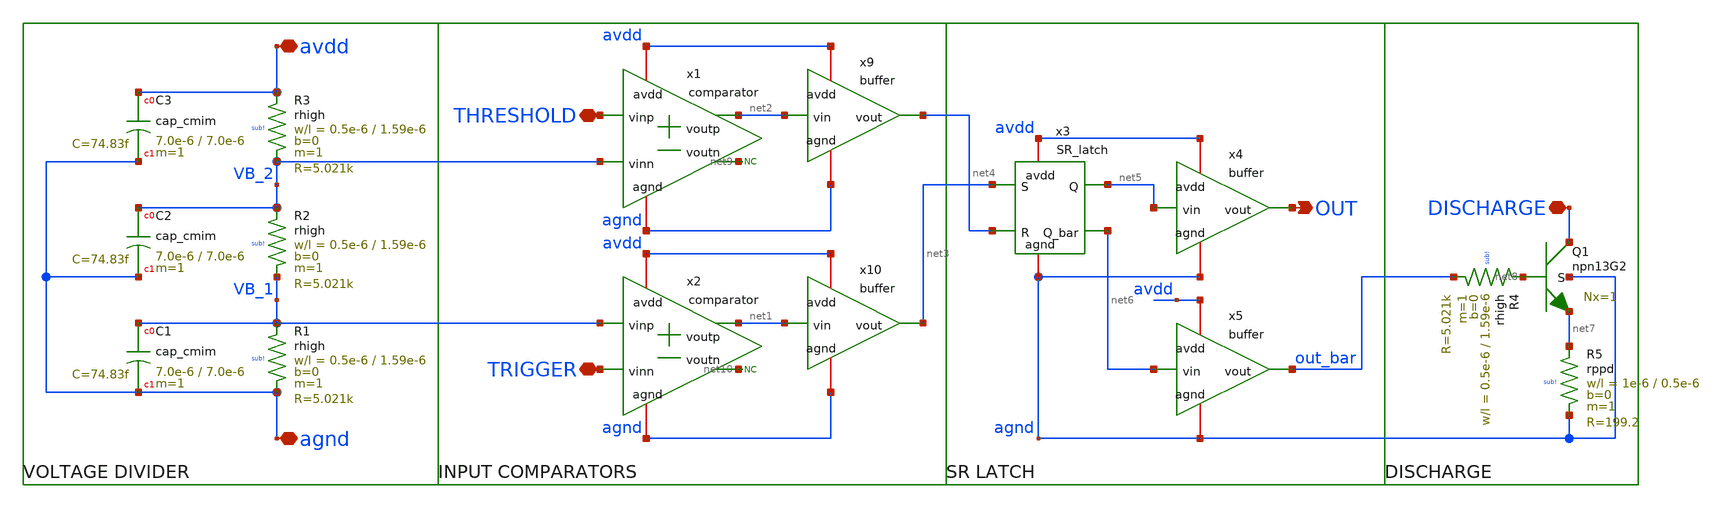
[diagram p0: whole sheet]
** sch_path: xschem/555.sch
**.subckt 555 OUT avdd agnd TRIGGER THRESHOLD DISCHARGE
*.opin OUT
*.iopin avdd
*.iopin agnd
*.iopin TRIGGER
*.iopin THRESHOLD
*.iopin DISCHARGE
XR3 avdd VB_2 sub! rhigh w=0.5e-6 l=1.59e-6 m=1 b=0 mm_ok=1
XR1 VB_1 agnd sub! rhigh w=0.5e-6 l=1.59e-6 m=1 b=0 mm_ok=1
XR2 VB_2 VB_1 sub! rhigh w=0.5e-6 l=1.59e-6 m=1 b=0 mm_ok=1
XC1 VB_1 agnd cap_cmim w=7.0e-6 l=7.0e-6 m=1 mm_ok=1
XC2 VB_2 agnd cap_cmim w=7.0e-6 l=7.0e-6 m=1 mm_ok=1
XC3 avdd agnd cap_cmim w=7.0e-6 l=7.0e-6 m=1 mm_ok=1
XR4 net8 out_bar sub! rhigh w=0.5e-6 l=1.59e-6 m=1 b=0 mm_ok=1
x1 avdd net2 net9 VB_2 THRESHOLD agnd comparator
x2 avdd net1 net10 TRIGGER VB_1 agnd comparator
x9 avdd net2 net4 agnd buffer
x10 avdd net1 net3 agnd buffer
x3 avdd net6 net5 agnd net3 net4 SR_latch
x4 avdd net5 OUT agnd buffer
x5 avdd net6 out_bar agnd buffer
* noconn #net9
* noconn #net10
XQ1 DISCHARGE net8 net7 agnd npn13G2 Nx=1 mm_ok=1
XR5 net7 agnd sub! rppd w=1e-6 l=0.5e-6 m=1 b=0 mm_ok=1
**.ends

* expanding   symbol:  comparator.sym # of pins=6
** sym_path: xschem/comparator.sym
** sch_path: xschem/comparator.sch
.subckt comparator avdd voutp voutn vinn vinp agnd
*.iopin avdd
*.ipin vinp
*.opin voutp
*.iopin agnd
*.ipin vinn
*.opin voutn
XQ1 voutp vinn net1 agnd npn13G2 Nx=1 mm_ok=1
XR1 avdd voutp sub! rppd w=0.5e-6 l=7.5e-6 m=1 b=0 mm_ok=1
XR2 net1 agnd sub! rppd w=0.5e-6 l=0.5e-6 m=1 b=0 mm_ok=1
XR3 avdd voutn sub! rppd w=0.5e-6 l=7.5e-6 m=1 b=0 mm_ok=1
XQ2 voutn vinp net1 agnd npn13G2 Nx=1 mm_ok=1
.ends


* expanding   symbol:  buffer.sym # of pins=4
** sym_path: xschem/buffer.sym
** sch_path: xschem/buffer.sch
.subckt buffer avdd vin vout agnd
*.iopin avdd
*.ipin vin
*.opin vout
*.iopin agnd
x1 avdd vin net1 agnd inverter
x2 avdd net1 vout agnd inverter
.ends


* expanding   symbol:  SR_latch.sym # of pins=6
** sym_path: xschem/SR_latch.sym
** sch_path: xschem/SR_latch.sch
.subckt SR_latch avdd Q_bar Q agnd S R
*.ipin R
*.opin Q_bar
*.ipin S
*.opin Q
*.iopin avdd
*.iopin agnd
XQ2 Q_bar net2 agnd agnd npn13G2 Nx=1 mm_ok=1
XQ1 Q net1 agnd agnd npn13G2 Nx=1 mm_ok=1
XR3 net1 R sub! rppd w=0.5e-6 l=20e-6 m=1 b=0 mm_ok=1
XR1 S net2 sub! rppd w=0.5e-6 l=20e-6 m=1 b=0 mm_ok=1
XR2 net1 agnd sub! rhigh w=0.5e-6 l=20e-6 m=1 b=0 mm_ok=1
XR4 net2 agnd sub! rhigh w=0.5e-6 l=20e-6 m=1 b=0 mm_ok=1
XR5 net2 Q sub! rppd w=0.5e-6 l=20e-6 m=1 b=0 mm_ok=1
XR6 Q_bar net1 sub! rppd w=0.5e-6 l=20e-6 m=1 b=0 mm_ok=1
XR7 avdd Q sub! rppd w=0.5e-6 l=2e-6 m=1 b=0 mm_ok=1
XR8 avdd Q_bar sub! rppd w=0.5e-6 l=2e-6 m=1 b=0 mm_ok=1
.ends


* expanding   symbol:  inverter.sym # of pins=4
** sym_path: xschem/inverter.sym
** sch_path: xschem/inverter.sch
.subckt inverter avdd vin vout agnd
*.iopin avdd
*.ipin vin
*.opin vout
*.iopin agnd
XQ1 vout base agnd agnd npn13G2 Nx=10 mm_ok=1
XR1 avdd vout sub! rhigh w=1e-6 l=0.5e-6 m=1 b=0 mm_ok=1
XR2 base vin sub! rhigh w=0.5e-6 l=0.5e-6 m=1 b=0 mm_ok=1
.ends

.end
